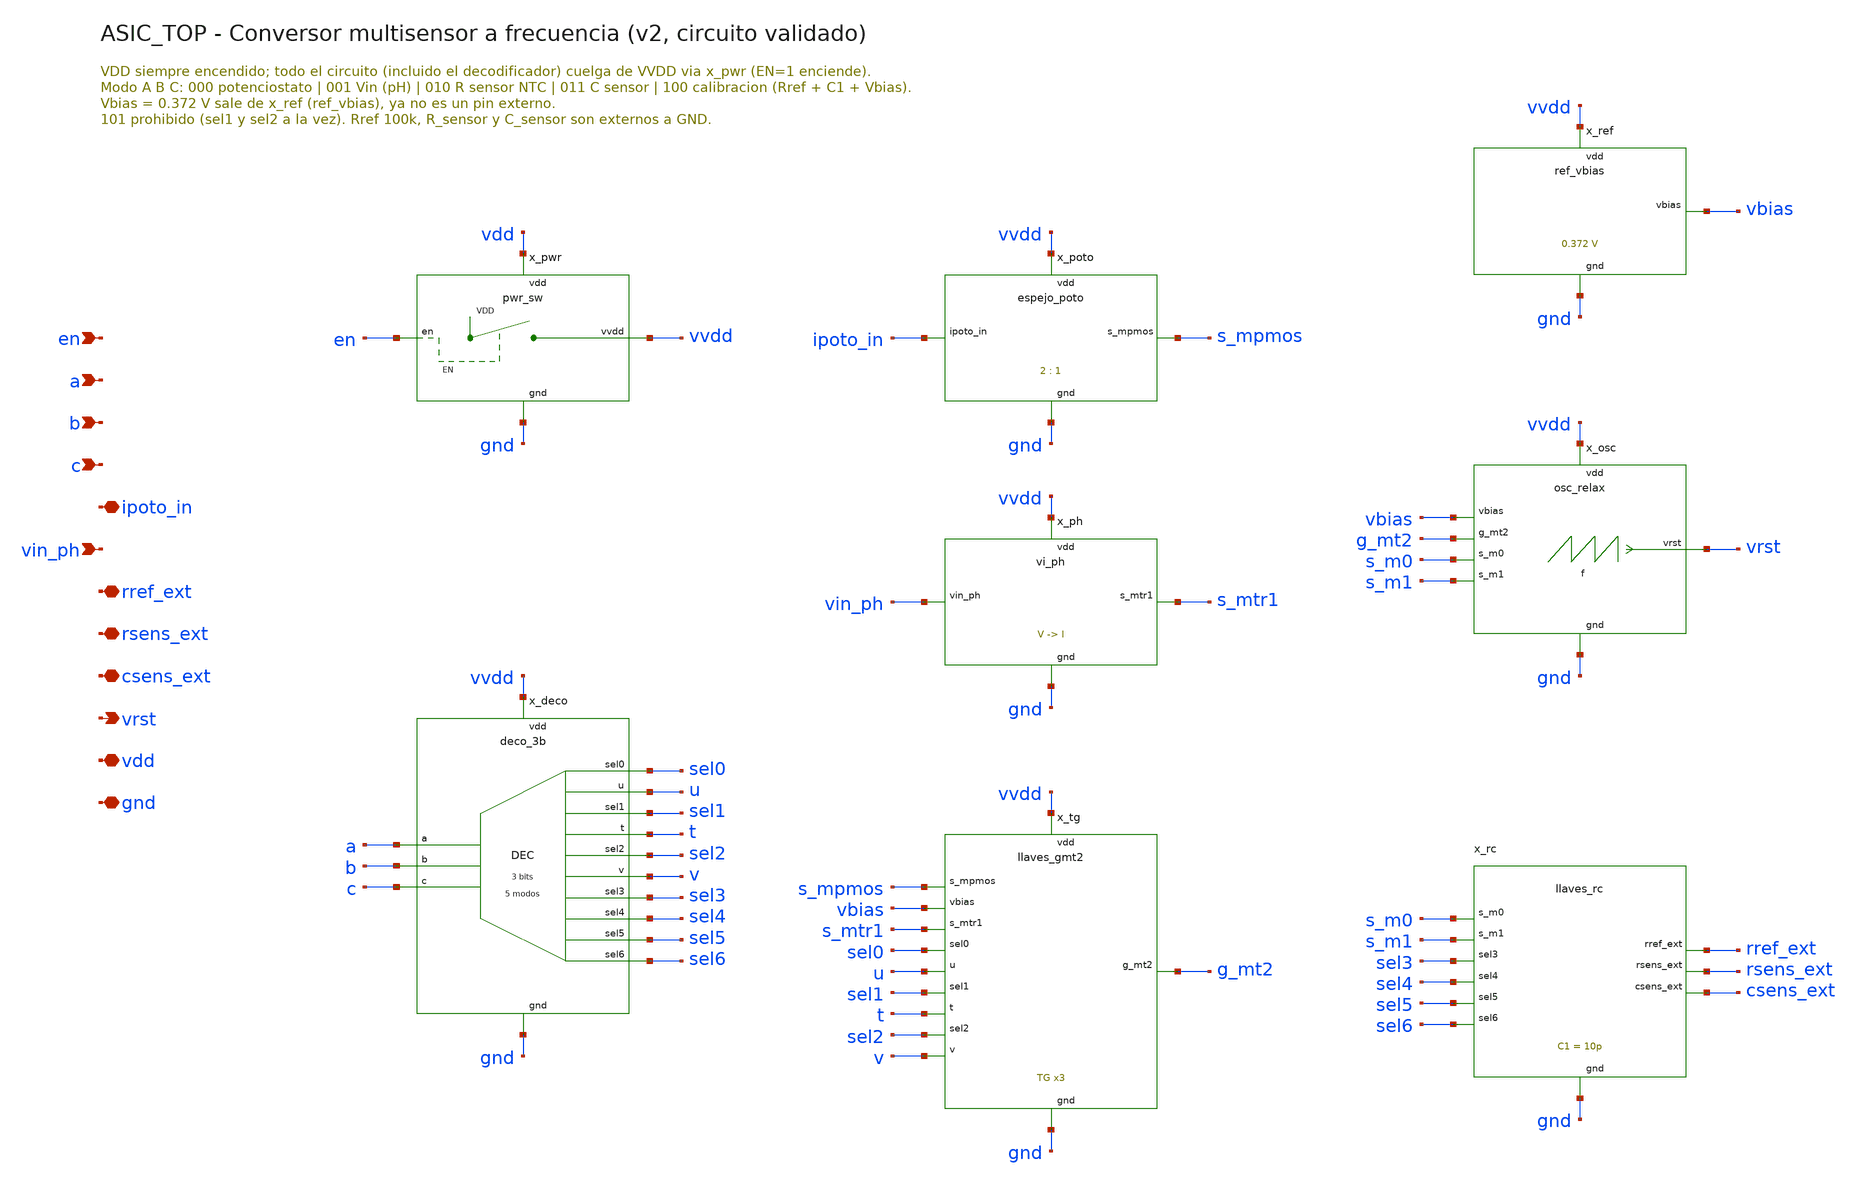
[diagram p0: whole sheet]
** sch_path: Enfoque_B/xschem/ASIC_TOP.sch
**.subckt ASIC_TOP en a b c ipoto_in vin_ph rref_ext rsens_ext csens_ext vrst vdd gnd
*.ipin en
*.ipin a
*.ipin b
*.ipin c
*.iopin ipoto_in
*.ipin vin_ph
*.iopin rref_ext
*.iopin rsens_ext
*.iopin csens_ext
*.opin vrst
*.iopin vdd
*.iopin gnd
x_pwr en vvdd vdd gnd pwr_sw
x_deco a b c sel0 u sel1 t sel2 v sel3 sel4 sel5 sel6 vvdd gnd deco_3b
x_poto ipoto_in s_mpmos vvdd gnd espejo_poto
x_ph vin_ph s_mtr1 vvdd gnd vi_ph
x_tg s_mpmos vbias s_mtr1 sel0 u sel1 t sel2 v g_mt2 vvdd gnd llaves_gmt2
x_ref vbias vvdd gnd ref_vbias
x_osc vbias g_mt2 s_m0 s_m1 vrst vvdd gnd osc_relax
x_rc s_m0 s_m1 sel3 sel4 sel5 sel6 rref_ext rsens_ext csens_ext gnd llaves_rc
**.ends

* expanding   symbol:  Enfoque_B/xschem/celdas/pwr_sw.sym # of pins=4
** sym_path: Enfoque_B/xschem/celdas/pwr_sw.sym
** sch_path: Enfoque_B/xschem/celdas/pwr_sw.sch
.subckt pwr_sw en vvdd vdd gnd
*.ipin en
*.opin vvdd
*.iopin vdd
*.iopin gnd
XMPi g en vdd vdd sg13_lv_pmos w=1u l=0.13u ng=1 m=1 mm_ok=1
XMNi g en gnd gnd sg13_lv_nmos w=0.3u l=4u ng=1 m=1 mm_ok=1
XCslew g gnd cap_cmim w=36.46e-6 l=36.46e-6 m=1 mm_ok=1
XMsw vvdd g vdd vdd sg13_lv_pmos w=40u l=0.13u ng=8 m=1 mm_ok=1
XMNpd vvdd g gnd gnd sg13_lv_nmos w=1u l=1u ng=1 m=1 mm_ok=1
.ends


* expanding   symbol:  Enfoque_B/xschem/celdas/deco_3b.sym # of pins=15
** sym_path: Enfoque_B/xschem/celdas/deco_3b.sym
** sch_path: Enfoque_B/xschem/celdas/deco_3b.sch
.subckt deco_3b a b c sel0 u sel1 t sel2 v sel3 sel4 sel5 sel6 vdd gnd
*.ipin a
*.ipin b
*.ipin c
*.opin sel0
*.opin u
*.opin sel1
*.opin t
*.opin sel2
*.opin v
*.opin sel3
*.opin sel4
*.opin sel5
*.opin sel6
*.iopin vdd
*.iopin gnd
XMP1 na a vdd vdd sg13_lv_pmos w=1u l=0.13u ng=1 m=1 mm_ok=1
XMN1 na a gnd gnd sg13_lv_nmos w=1u l=0.13u ng=1 m=1 mm_ok=1
XMP2 nb b vdd vdd sg13_lv_pmos w=1u l=0.13u ng=1 m=1 mm_ok=1
XMN2 nb b gnd gnd sg13_lv_nmos w=1u l=0.13u ng=1 m=1 mm_ok=1
XMP3 nc c vdd vdd sg13_lv_pmos w=1u l=0.13u ng=1 m=1 mm_ok=1
XMN3 nc c gnd gnd sg13_lv_nmos w=1u l=0.13u ng=1 m=1 mm_ok=1
XMP4 sel1 na vdd vdd sg13_lv_pmos w=1u l=0.13u ng=1 m=1 mm_ok=1
XMP5 sel1 nb vdd vdd sg13_lv_pmos w=1u l=0.13u ng=1 m=1 mm_ok=1
XMN4 sel1 na x1 gnd sg13_lv_nmos w=1u l=0.13u ng=1 m=1 mm_ok=1
XMN5 x1 nb gnd gnd sg13_lv_nmos w=1u l=0.13u ng=1 m=1 mm_ok=1
XMP6 t sel1 vdd vdd sg13_lv_pmos w=1u l=0.13u ng=1 m=1 mm_ok=1
XMN6 t sel1 gnd gnd sg13_lv_nmos w=1u l=0.13u ng=1 m=1 mm_ok=1
XMP7 u t vdd vdd sg13_lv_pmos w=1u l=0.13u ng=1 m=1 mm_ok=1
XMP8 u nc vdd vdd sg13_lv_pmos w=1u l=0.13u ng=1 m=1 mm_ok=1
XMN7 u t x2 gnd sg13_lv_nmos w=1u l=0.13u ng=1 m=1 mm_ok=1
XMN8 x2 nc gnd gnd sg13_lv_nmos w=1u l=0.13u ng=1 m=1 mm_ok=1
XMP9 sel0 u vdd vdd sg13_lv_pmos w=1u l=0.13u ng=1 m=1 mm_ok=1
XMN9 sel0 u gnd gnd sg13_lv_nmos w=1u l=0.13u ng=1 m=1 mm_ok=1
XMP10 v nb vdd vdd sg13_lv_pmos w=1u l=0.13u ng=1 m=1 mm_ok=1
XMP11 v c vdd vdd sg13_lv_pmos w=1u l=0.13u ng=1 m=1 mm_ok=1
XMN10 v nb x3 gnd sg13_lv_nmos w=1u l=0.13u ng=1 m=1 mm_ok=1
XMN11 x3 c gnd gnd sg13_lv_nmos w=1u l=0.13u ng=1 m=1 mm_ok=1
XMP12 sel2 v vdd vdd sg13_lv_pmos w=1u l=0.13u ng=1 m=1 mm_ok=1
XMN12 sel2 v gnd gnd sg13_lv_nmos w=1u l=0.13u ng=1 m=1 mm_ok=1
XMP13 sel3 b vdd vdd sg13_lv_pmos w=1u l=0.13u ng=1 m=1 mm_ok=1
XMP14 sel3 nc vdd vdd sg13_lv_pmos w=1u l=0.13u ng=1 m=1 mm_ok=1
XMN13 sel3 b x4 gnd sg13_lv_nmos w=1u l=0.13u ng=1 m=1 mm_ok=1
XMN14 x4 nc gnd gnd sg13_lv_nmos w=1u l=0.13u ng=1 m=1 mm_ok=1
XMP15 sel4 sel3 vdd vdd sg13_lv_pmos w=1u l=0.13u ng=1 m=1 mm_ok=1
XMN15 sel4 sel3 gnd gnd sg13_lv_nmos w=1u l=0.13u ng=1 m=1 mm_ok=1
XMP16 sel5 b vdd vdd sg13_lv_pmos w=1u l=0.13u ng=1 m=1 mm_ok=1
XMP17 sel5 c vdd vdd sg13_lv_pmos w=1u l=0.13u ng=1 m=1 mm_ok=1
XMN16 sel5 b x5 gnd sg13_lv_nmos w=1u l=0.13u ng=1 m=1 mm_ok=1
XMN17 x5 c gnd gnd sg13_lv_nmos w=1u l=0.13u ng=1 m=1 mm_ok=1
XMP18 sel6 sel5 vdd vdd sg13_lv_pmos w=1u l=0.13u ng=1 m=1 mm_ok=1
XMN18 sel6 sel5 gnd gnd sg13_lv_nmos w=1u l=0.13u ng=1 m=1 mm_ok=1
.ends


* expanding   symbol:  Enfoque_B/xschem/celdas/espejo_poto.sym # of pins=4
** sym_path: Enfoque_B/xschem/celdas/espejo_poto.sym
** sch_path: Enfoque_B/xschem/celdas/espejo_poto.sch
.subckt espejo_poto ipoto_in s_mpmos vdd gnd
*.iopin ipoto_in
*.opin s_mpmos
*.iopin vdd
*.iopin gnd
XM_in ipoto_in ipoto_in gnd gnd sg13_lv_nmos w=5.1u l=1.2u ng=1 m=1 mm_ok=1
XM_out s_mpmos ipoto_in gnd gnd sg13_lv_nmos w=2.55u l=1.2u ng=1 m=1 mm_ok=1
XM_pmos s_mpmos s_mpmos vdd vdd sg13_lv_pmos w=2u l=1u ng=1 m=1 mm_ok=1
.ends


* expanding   symbol:  Enfoque_B/xschem/celdas/vi_ph.sym # of pins=4
** sym_path: Enfoque_B/xschem/celdas/vi_ph.sym
** sch_path: Enfoque_B/xschem/celdas/vi_ph.sch
.subckt vi_ph vin_ph s_mtr1 vdd gnd
*.ipin vin_ph
*.opin s_mtr1
*.iopin vdd
*.iopin gnd
XMTR1 s_mtr1 s_mtr1 vdd vdd sg13_lv_pmos w=1u l=0.34u ng=1 m=1 mm_ok=1
XMTR2 s_mtr1 vin_ph n_tr gnd sg13_lv_nmos w=1u l=10u ng=1 m=1 mm_ok=1
XMTR3 n_tr vdd gnd gnd sg13_lv_nmos w=10u l=0.34u ng=1 m=1 mm_ok=1
.ends


* expanding   symbol:  Enfoque_B/xschem/celdas/llaves_gmt2.sym # of pins=12
** sym_path: Enfoque_B/xschem/celdas/llaves_gmt2.sym
** sch_path: Enfoque_B/xschem/celdas/llaves_gmt2.sch
.subckt llaves_gmt2 s_mpmos vbias s_mtr1 sel0 u sel1 t sel2 v g_mt2 vdd gnd
*.iopin s_mpmos
*.iopin vbias
*.iopin s_mtr1
*.ipin sel0
*.ipin u
*.ipin sel1
*.ipin t
*.ipin sel2
*.ipin v
*.iopin g_mt2
*.iopin vdd
*.iopin gnd
XMN19 s_mpmos sel0 g_mt2 gnd sg13_lv_nmos w=0.15u l=0.13u ng=1 m=1 mm_ok=1
XMP19 s_mpmos u g_mt2 vdd sg13_lv_pmos w=0.15u l=0.13u ng=1 m=1 mm_ok=1
XMN20 vbias sel1 g_mt2 gnd sg13_lv_nmos w=0.15u l=0.13u ng=1 m=1 mm_ok=1
XMP20 vbias t g_mt2 vdd sg13_lv_pmos w=0.15u l=0.13u ng=1 m=1 mm_ok=1
XMN21 s_mtr1 sel2 g_mt2 gnd sg13_lv_nmos w=0.15u l=0.13u ng=1 m=1 mm_ok=1
XMP21 s_mtr1 v g_mt2 vdd sg13_lv_pmos w=0.15u l=0.13u ng=1 m=1 mm_ok=1
.ends


* expanding   symbol:  Enfoque_B/xschem/celdas/ref_vbias.sym # of pins=3
** sym_path: Enfoque_B/xschem/celdas/ref_vbias.sym
** sch_path: Enfoque_B/xschem/celdas/ref_vbias.sch
.subckt ref_vbias vbias vdd gnd
*.opin vbias
*.iopin vdd
*.iopin gnd
XMtop vbias vbias vdd vdd sg13_lv_pmos w=2u l=1u ng=1 m=1 mm_ok=1
XMbot vbias vdd gnd gnd sg13_lv_nmos w=0.15u l=2.2u ng=1 m=1 mm_ok=1
.ends


* expanding   symbol:  Enfoque_B/xschem/celdas/osc_relax.sym # of pins=7
** sym_path: Enfoque_B/xschem/celdas/osc_relax.sym
** sch_path: Enfoque_B/xschem/celdas/osc_relax.sch
.subckt osc_relax vbias g_mt2 s_m0 s_m1 vrst vdd gnd
*.ipin vbias
*.ipin g_mt2
*.iopin s_m0
*.iopin s_m1
*.opin vrst
*.iopin vdd
*.iopin gnd
XMT3 n_ref vbias vdd vdd sg13_lv_pmos w=2u l=1u ng=1 m=1 mm_ok=1
XMT2 n_cmp g_mt2 vdd vdd sg13_lv_pmos w=2u l=1u ng=1 m=1 mm_ok=1
XM0 n_ref n_ref s_m0 gnd sg13_lv_nmos w=5.1u l=1.2u ng=1 m=1 mm_ok=1
XM1 n_cmp n_ref s_m1 gnd sg13_lv_nmos w=5.1u l=1.2u ng=1 m=1 mm_ok=1
XMpbuf1 n_buf n_cmp vdd vdd sg13_lv_pmos w=1u l=0.34u ng=1 m=1 mm_ok=1
XMnbuf1 n_buf n_cmp gnd gnd sg13_lv_nmos w=0.5u l=0.34u ng=1 m=1 mm_ok=1
XCD n_buf gnd cap_cmim w=44.67e-6 l=44.67e-6 m=1 mm_ok=1
XMpbuf2 vrst n_buf vdd vdd sg13_lv_pmos w=1u l=0.34u ng=1 m=1 mm_ok=1
XMnbuf2 vrst n_buf gnd gnd sg13_lv_nmos w=0.5u l=0.34u ng=1 m=1 mm_ok=1
XMs1 s_m1 vrst gnd gnd sg13_lv_nmos w=60u l=1.2u ng=12 m=1 mm_ok=1
.ends


* expanding   symbol:  Enfoque_B/xschem/celdas/llaves_rc.sym # of pins=10
** sym_path: Enfoque_B/xschem/celdas/llaves_rc.sym
** sch_path: Enfoque_B/xschem/celdas/llaves_rc.sch
.subckt llaves_rc s_m0 s_m1 sel3 sel4 sel5 sel6 rref_ext rsens_ext csens_ext gnd
*.iopin s_m0
*.iopin s_m1
*.ipin sel3
*.ipin sel4
*.ipin sel5
*.ipin sel6
*.iopin rref_ext
*.iopin rsens_ext
*.iopin csens_ext
*.iopin gnd
XMN22 s_m0 sel3 rref_ext gnd sg13_lv_nmos w=5u l=0.34u ng=1 m=1 mm_ok=1
XMN23 s_m0 sel4 rsens_ext gnd sg13_lv_nmos w=5u l=0.34u ng=1 m=1 mm_ok=1
XMN24 s_m1 sel5 c1_int gnd sg13_lv_nmos w=5u l=0.34u ng=1 m=1 mm_ok=1
XMN25 s_m1 sel6 csens_ext gnd sg13_lv_nmos w=5u l=0.34u ng=1 m=1 mm_ok=1
XC1 c1_int gnd cap_cmim w=57.68e-6 l=57.68e-6 m=2 mm_ok=1
.ends

.end
